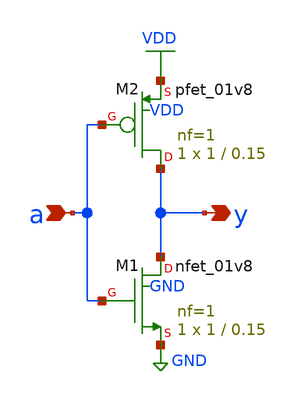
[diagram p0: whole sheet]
** sch_path: xschem/inverter.sch
**.subckt inverter a y
*.ipin a
*.opin y
XM1 y a GND GND sky130_fd_pr__nfet_01v8 L=0.15 W=1 nf=1 ad='int((1 + 1)/2) * 1 / 1 * 0.29' as='int((1 + 2)/2) * 1 / 1 * 0.29'
+ pd='2*int((1 + 1)/2) * (1 / 1 + 0.29)' ps='2*int((1 + 2)/2) * (1 / 1 + 0.29)' nrd='0.29 / 1 ' nrs='0.29 / 1 '
+ sa=0 sb=0 sd=0 mult=1 m=1
XM2 y a VDD VDD sky130_fd_pr__pfet_01v8 L=0.15 W=1 nf=1 ad='int((1 + 1)/2) * 1 / 1 * 0.29' as='int((1 + 2)/2) * 1 / 1 * 0.29'
+ pd='2*int((1 + 1)/2) * (1 / 1 + 0.29)' ps='2*int((1 + 2)/2) * (1 / 1 + 0.29)' nrd='0.29 / 1 ' nrs='0.29 / 1 '
+ sa=0 sb=0 sd=0 mult=1 m=1
**.ends
.GLOBAL VDD
.GLOBAL GND
.end
